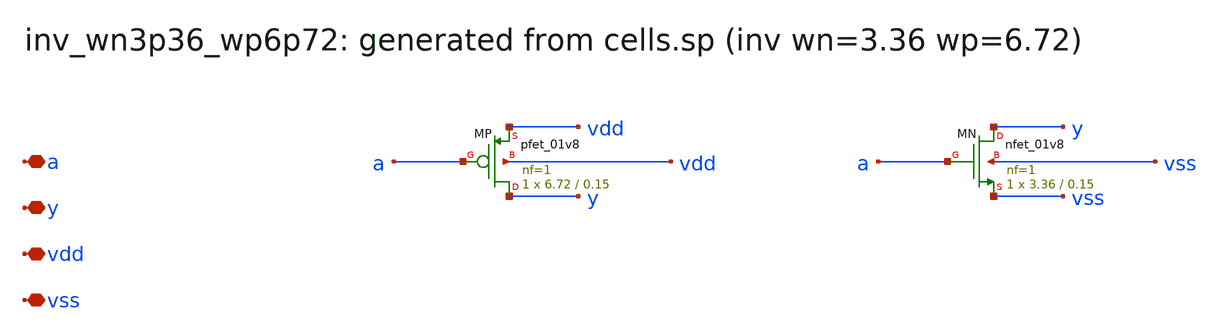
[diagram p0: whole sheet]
** sch_path: sram/xschem/inv_wn3p36_wp6p72.sch
**.subckt inv_wn3p36_wp6p72 a y vdd vss
*.iopin a
*.iopin y
*.iopin vdd
*.iopin vss
XMP y a vdd vdd sky130_fd_pr__pfet_01v8 L=0.15 W=6.72 nf=1 ad='int((nf+1)/2) * W/nf * 0.29' as='int((nf+2)/2) * W/nf * 0.29'
+ pd='2*int((nf+1)/2) * (W/nf + 0.29)' ps='2*int((nf+2)/2) * (W/nf + 0.29)' nrd='0.29 / W' nrs='0.29 / W'
+ sa=0 sb=0 sd=0 mult=1 m=1
XMN y a vss vss sky130_fd_pr__nfet_01v8 L=0.15 W=3.36 nf=1 ad='int((1 + 1)/2) * 3.36 / 1 * 0.29' as='int((1 + 2)/2) * 3.36 / 1 * 0.29'
+ pd='2*int((1 + 1)/2) * (3.36 / 1 + 0.29)' ps='2*int((1 + 2)/2) * (3.36 / 1 + 0.29)' nrd='0.29 / 3.36 '
+ nrs='0.29 / 3.36 ' sa=0 sb=0 sd=0 mult=1 m=1
**.ends
.end
